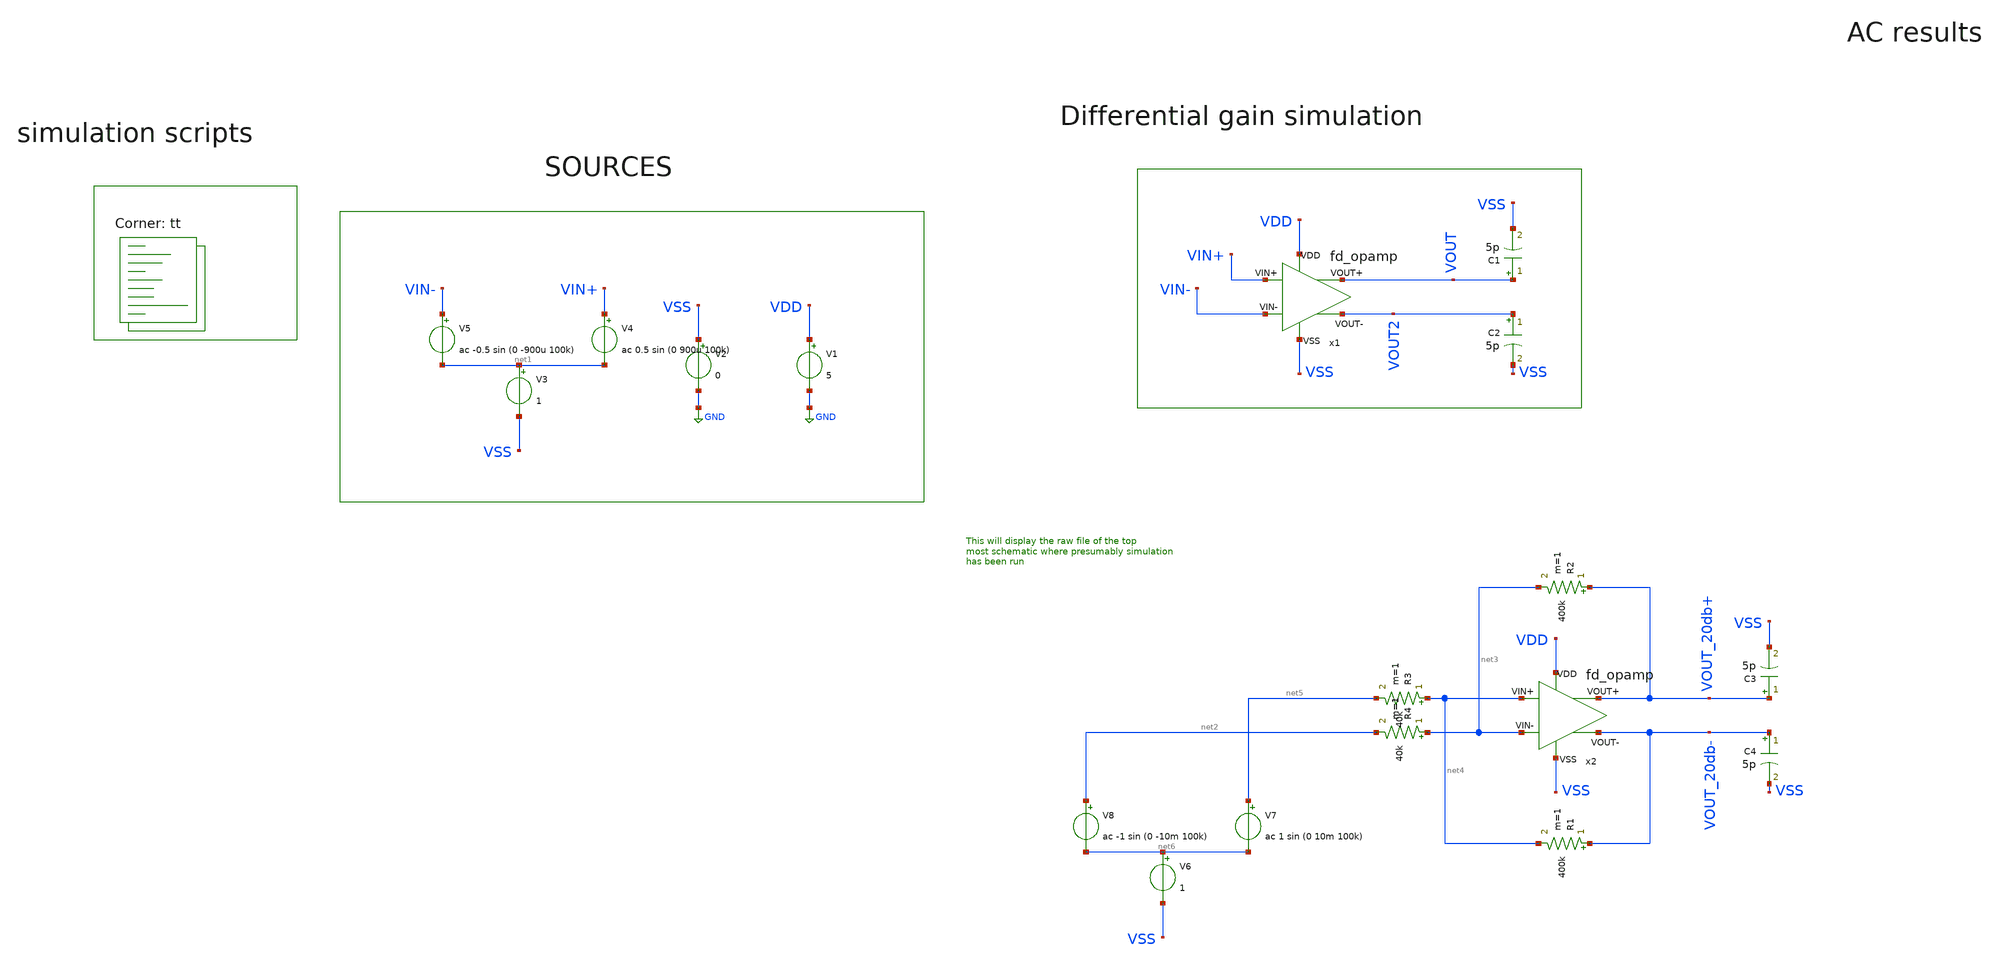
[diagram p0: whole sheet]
** sch_path: my_ip/testbenches_sky/fully_differential_telescopic_cascode_5V_V1/tb/tb.sch
**.subckt tb
V1 VDD GND 5
V2 VSS GND 0
V3 net1 VSS 1
V4 VIN+ net1 ac 0.5 sin (0 900u 100k)
V5 VIN- net1 ac -0.5 sin (0 -900u 100k)
C1 VOUT VSS 5p m=1
C2 VOUT2 VSS 5p m=1
x1 VDD VSS VIN+ VOUT VIN- VOUT2 fd_opamp
C3 VOUT_20db+ VSS 5p m=1
C4 VOUT_20db- VSS 5p m=1
x2 VDD VSS net4 VOUT_20db+ net3 VOUT_20db- fd_opamp
R2 VOUT_20db+ net3 400k m=1
R3 net4 net5 40k m=1
R1 VOUT_20db- net4 400k m=1
R4 net3 net2 40k m=1
V6 net6 VSS 1
V7 net5 net6 ac 1 sin (0 10m 100k)
V8 net2 net6 ac -1 sin (0 -10m 100k)
**** begin user architecture code
.lib $::SKYWATER_MODELS/sky130.lib.spice tt
**** end user architecture code
**.ends
.GLOBAL GND
**** begin user architecture code


* ngspice commands
.options savecurrents
.TEMP 27
.control
save all
save @m.x1.xm1.msky130_fd_pr__pfet_g5v0d10v5[gm]
save @m.x1.xm1.msky130_fd_pr__pfet_g5v0d10v5[vth]
save @m.x1.xm1.msky130_fd_pr__pfet_g5v0d10v5[vds]
save @m.x1.xm1.msky130_fd_pr__pfet_g5v0d10v5[vgs]

save @m.x1.xm2.msky130_fd_pr__pfet_g5v0d10v5[gm]
save @m.x1.xm2.msky130_fd_pr__pfet_g5v0d10v5[vth]
save @m.x1.xm2.msky130_fd_pr__pfet_g5v0d10v5[vds]
save @m.x1.xm2.msky130_fd_pr__pfet_g5v0d10v5[vgs]

save @m.x1.xm3.msky130_fd_pr__pfet_g5v0d10v5[gm]
save @m.x1.xm3.msky130_fd_pr__pfet_g5v0d10v5[vth]
save @m.x1.xm3.msky130_fd_pr__pfet_g5v0d10v5[vds]
save @m.x1.xm3.msky130_fd_pr__pfet_g5v0d10v5[vgs]

save @m.x1.xm4.msky130_fd_pr__pfet_g5v0d10v5[gm]
save @m.x1.xm4.msky130_fd_pr__pfet_g5v0d10v5[vth]
save @m.x1.xm4.msky130_fd_pr__pfet_g5v0d10v5[vds]
save @m.x1.xm4.msky130_fd_pr__pfet_g5v0d10v5[vgs]

save @m.x1.xm5.msky130_fd_pr__nfet_g5v0d10v5[gm]
save @m.x1.xm5.msky130_fd_pr__nfet_g5v0d10v5[vth]
save @m.x1.xm5.msky130_fd_pr__nfet_g5v0d10v5[vds]
save @m.x1.xm5.msky130_fd_pr__nfet_g5v0d10v5[vgs]

save @m.x1.xm6.msky130_fd_pr__nfet_g5v0d10v5[gm]
save @m.x1.xm6.msky130_fd_pr__nfet_g5v0d10v5[vth]
save @m.x1.xm6.msky130_fd_pr__nfet_g5v0d10v5[vds]
save @m.x1.xm6.msky130_fd_pr__nfet_g5v0d10v5[vgs]

save @m.x1.xm7.msky130_fd_pr__nfet_g5v0d10v5[gm]
save @m.x1.xm7.msky130_fd_pr__nfet_g5v0d10v5[vth]
save @m.x1.xm7.msky130_fd_pr__nfet_g5v0d10v5[vds]
save @m.x1.xm7.msky130_fd_pr__nfet_g5v0d10v5[vgs]

save @m.x1.xm8.msky130_fd_pr__nfet_g5v0d10v5[gm]
save @m.x1.xm8.msky130_fd_pr__nfet_g5v0d10v5[vth]
save @m.x1.xm8.msky130_fd_pr__nfet_g5v0d10v5[vds]
save @m.x1.xm8.msky130_fd_pr__nfet_g5v0d10v5[vgs]

save @m.x1.xm9.msky130_fd_pr__pfet_g5v0d10v5[gm]
save @m.x1.xm9.msky130_fd_pr__pfet_g5v0d10v5[vth]
save @m.x1.xm9.msky130_fd_pr__pfet_g5v0d10v5[vds]
save @m.x1.xm9.msky130_fd_pr__pfet_g5v0d10v5[vgs]

save @m.x1.xm10.msky130_fd_pr__pfet_g5v0d10v5[gm]
save @m.x1.xm10.msky130_fd_pr__pfet_g5v0d10v5[vth]
save @m.x1.xm10.msky130_fd_pr__pfet_g5v0d10v5[vds]
save @m.x1.xm10.msky130_fd_pr__pfet_g5v0d10v5[vgs]

save @m.x1.xm11.msky130_fd_pr__pfet_g5v0d10v5[gm]
save @m.x1.xm11.msky130_fd_pr__pfet_g5v0d10v5[vth]
save @m.x1.xm11.msky130_fd_pr__pfet_g5v0d10v5[vds]
save @m.x1.xm11.msky130_fd_pr__pfet_g5v0d10v5[vgs]

save @m.x1.xm12.msky130_fd_pr__pfet_g5v0d10v5[gm]
save @m.x1.xm12.msky130_fd_pr__pfet_g5v0d10v5[vth]
save @m.x1.xm12.msky130_fd_pr__pfet_g5v0d10v5[vds]
save @m.x1.xm12.msky130_fd_pr__pfet_g5v0d10v5[vgs]

save @m.x1.xm13.msky130_fd_pr__nfet_g5v0d10v5[gm]
save @m.x1.xm13.msky130_fd_pr__nfet_g5v0d10v5[vth]
save @m.x1.xm13.msky130_fd_pr__nfet_g5v0d10v5[vds]
save @m.x1.xm13.msky130_fd_pr__nfet_g5v0d10v5[vgs]

save @m.x1.xm14.msky130_fd_pr__nfet_g5v0d10v5[gm]
save @m.x1.xm14.msky130_fd_pr__nfet_g5v0d10v5[vth]
save @m.x1.xm14.msky130_fd_pr__nfet_g5v0d10v5[vds]
save @m.x1.xm14.msky130_fd_pr__nfet_g5v0d10v5[vgs]

save @m.x1.xm15.msky130_fd_pr__nfet_g5v0d10v5[gm]
save @m.x1.xm15.msky130_fd_pr__nfet_g5v0d10v5[vth]
save @m.x1.xm15.msky130_fd_pr__nfet_g5v0d10v5[vds]
save @m.x1.xm15.msky130_fd_pr__nfet_g5v0d10v5[vgs]

save @m.x1.xm16.msky130_fd_pr__nfet_g5v0d10v5[gm]
save @m.x1.xm16.msky130_fd_pr__nfet_g5v0d10v5[vth]
save @m.x1.xm16.msky130_fd_pr__nfet_g5v0d10v5[vds]
save @m.x1.xm16.msky130_fd_pr__nfet_g5v0d10v5[vgs]


save @m.x1.xm17.msky130_fd_pr__pfet_g5v0d10v5[gm]
save @m.x1.xm17.msky130_fd_pr__pfet_g5v0d10v5[vth]
save @m.x1.xm17.msky130_fd_pr__pfet_g5v0d10v5[vds]
save @m.x1.xm17.msky130_fd_pr__pfet_g5v0d10v5[vgs]

save @m.x1.xm18.msky130_fd_pr__pfet_g5v0d10v5[gm]
save @m.x1.xm18.msky130_fd_pr__pfet_g5v0d10v5[vth]
save @m.x1.xm18.msky130_fd_pr__pfet_g5v0d10v5[vds]
save @m.x1.xm18.msky130_fd_pr__pfet_g5v0d10v5[vgs]

save @m.x1.xm19.msky130_fd_pr__pfet_g5v0d10v5[gm]
save @m.x1.xm19.msky130_fd_pr__pfet_g5v0d10v5[vth]
save @m.x1.xm19.msky130_fd_pr__pfet_g5v0d10v5[vds]
save @m.x1.xm19.msky130_fd_pr__pfet_g5v0d10v5[vgs]

save @m.x1.xm20.msky130_fd_pr__pfet_g5v0d10v5[gm]
save @m.x1.xm20.msky130_fd_pr__pfet_g5v0d10v5[vth]
save @m.x1.xm20.msky130_fd_pr__pfet_g5v0d10v5[vds]
save @m.x1.xm20.msky130_fd_pr__pfet_g5v0d10v5[vgs]

save @m.x1.xm21.msky130_fd_pr__pfet_g5v0d10v5[gm]
save @m.x1.xm21.msky130_fd_pr__pfet_g5v0d10v5[vth]
save @m.x1.xm21.msky130_fd_pr__pfet_g5v0d10v5[vds]
save @m.x1.xm21.msky130_fd_pr__pfet_g5v0d10v5[vgs]

save @m.x1.xm22.msky130_fd_pr__pfet_g5v0d10v5[gm]
save @m.x1.xm22.msky130_fd_pr__pfet_g5v0d10v5[vth]
save @m.x1.xm22.msky130_fd_pr__pfet_g5v0d10v5[vds]
save @m.x1.xm22.msky130_fd_pr__pfet_g5v0d10v5[vgs]

save @m.x1.xm23.msky130_fd_pr__nfet_g5v0d10v5[gm]
save @m.x1.xm23.msky130_fd_pr__nfet_g5v0d10v5[vth]
save @m.x1.xm23.msky130_fd_pr__nfet_g5v0d10v5[vds]
save @m.x1.xm23.msky130_fd_pr__nfet_g5v0d10v5[vgs]

save @m.x1.xm24.msky130_fd_pr__nfet_g5v0d10v5[gm]
save @m.x1.xm24.msky130_fd_pr__nfet_g5v0d10v5[vth]
save @m.x1.xm24.msky130_fd_pr__nfet_g5v0d10v5[vds]
save @m.x1.xm24.msky130_fd_pr__nfet_g5v0d10v5[vgs]

save @m.x1.xm25.msky130_fd_pr__nfet_g5v0d10v5[gm]
save @m.x1.xm25.msky130_fd_pr__nfet_g5v0d10v5[vth]
save @m.x1.xm25.msky130_fd_pr__nfet_g5v0d10v5[vds]
save @m.x1.xm25.msky130_fd_pr__nfet_g5v0d10v5[vgs]

save @m.x1.xm26.msky130_fd_pr__pfet_g5v0d10v5[gm]
save @m.x1.xm26.msky130_fd_pr__pfet_g5v0d10v5[vth]
save @m.x1.xm26.msky130_fd_pr__pfet_g5v0d10v5[vds]
save @m.x1.xm26.msky130_fd_pr__pfet_g5v0d10v5[vgs]

save @m.x1.xm27.msky130_fd_pr__pfet_g5v0d10v5[gm]
save @m.x1.xm27.msky130_fd_pr__pfet_g5v0d10v5[vth]
save @m.x1.xm27.msky130_fd_pr__pfet_g5v0d10v5[vds]
save @m.x1.xm27.msky130_fd_pr__pfet_g5v0d10v5[vgs]

save @m.x1.xm28.msky130_fd_pr__nfet_g5v0d10v5[gm]
save @m.x1.xm28.msky130_fd_pr__nfet_g5v0d10v5[vth]
save @m.x1.xm28.msky130_fd_pr__nfet_g5v0d10v5[vds]
save @m.x1.xm28.msky130_fd_pr__nfet_g5v0d10v5[vgs]

op
set appendwrite
write tb.raw

ac dec 10 1 50G
plot db(v(VOUT)) (180*ph(v(VOUT))/pi)
plot db(v(VOUT_20db+))
set appendwrite
write tb.raw

tran 1ns 100u
plot v(VOUT) v(VOUT2)
plot v(VOUT_20db+)
set appendwrite
write tb.raw
.endc



**** end user architecture code
.end
